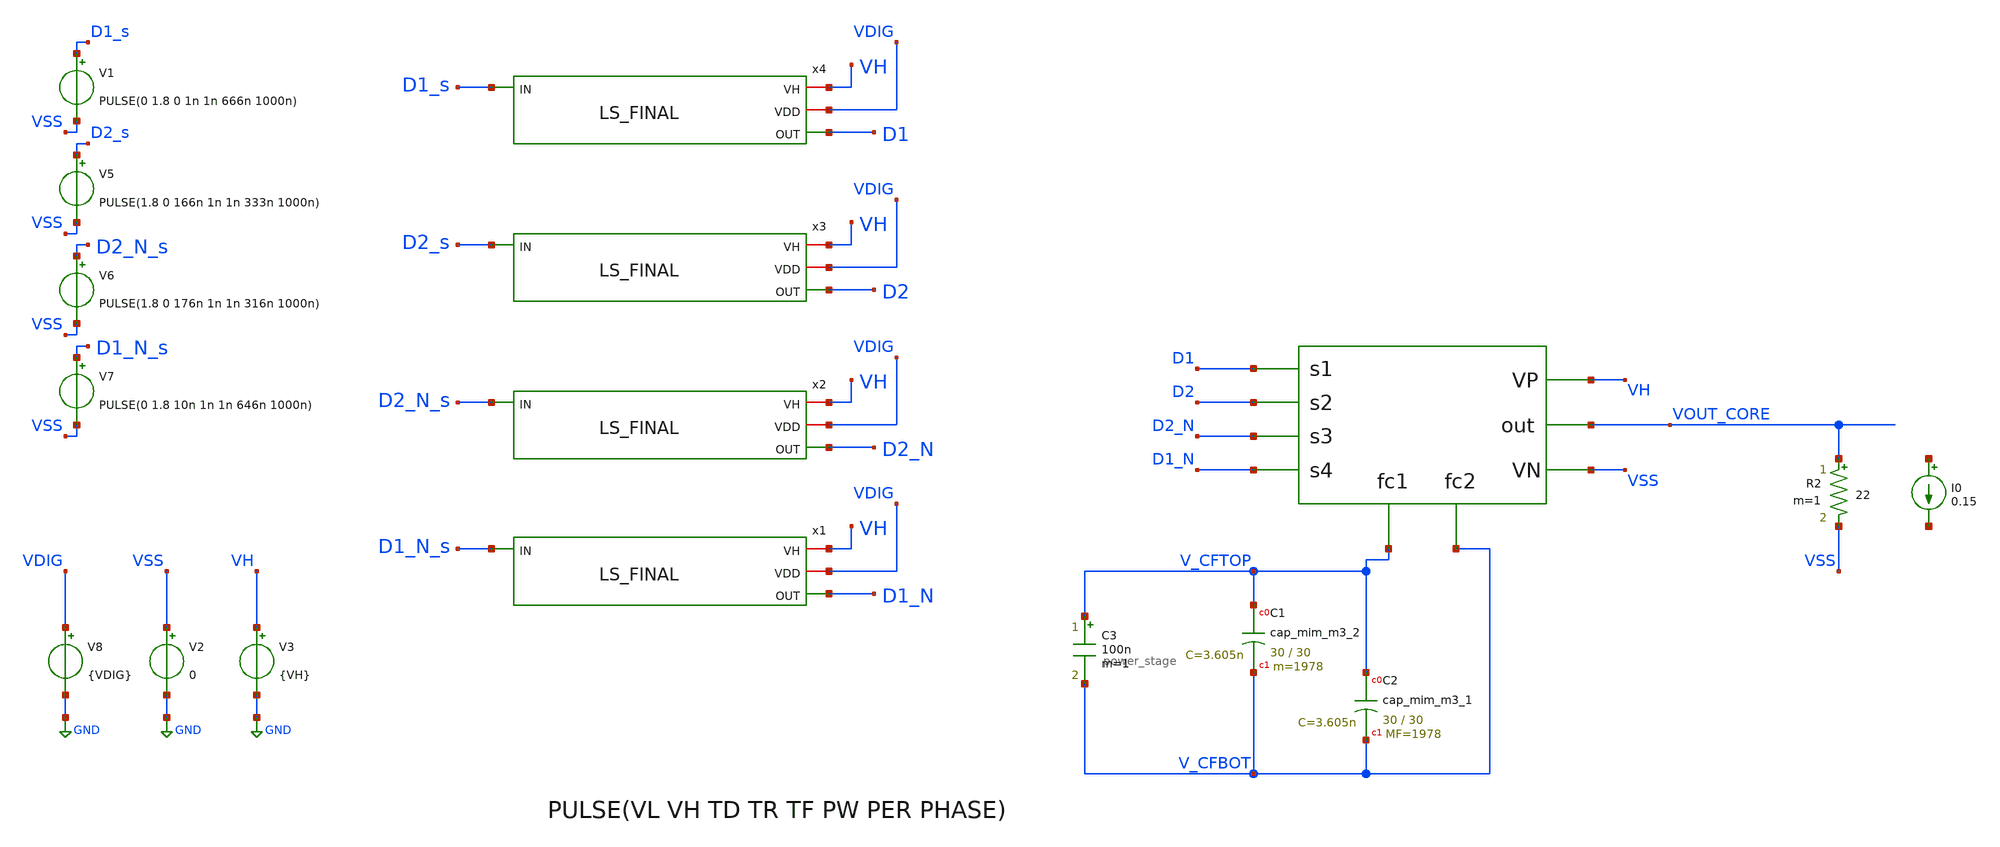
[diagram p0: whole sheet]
** sch_path: xschem/testbench/Interleaved/interleaved_testbench_tomas.sch
**.subckt interleaved_testbench_tomas
V2 VSS GND 0
V3 VH GND {VH}
I0 net1 net2 0.15
R2 VOUT_CORE VSS 22 m=1
XC1 V_CFTOP V_CFBOT sky130_fd_pr__cap_mim_m3_2 W=30 L=30 MF=1978 m=1978
XC2 V_CFTOP V_CFBOT sky130_fd_pr__cap_mim_m3_1 W=30 L=30 MF=1978 m=1978
X2v D1 D2 D2_N D1_N V_CFTOP V_CFBOT VOUT_CORE VH VSS power_stage
V8 VDIG GND {VDIG}
x1 VH VDIG D1_N D1_N_s LS_FINAL
x2 VH VDIG D2_N D2_N_s LS_FINAL
x3 VH VDIG D2 D2_s LS_FINAL
x4 VH VDIG D1 D1_s LS_FINAL
V6 D2_N_s VSS PULSE(1.8 0 176n 1n 1n 316n 1000n)
V5 D2_s VSS PULSE(1.8 0 166n 1n 1n 333n 1000n)
V7 D1_N_s VSS PULSE(0 1.8 10n 1n 1n 646n 1000n)
V1 D1_s VSS PULSE(0 1.8 0 1n 1n 666n 1000n)
C3 V_CFTOP V_CFBOT 100n m=1
**** begin user architecture code


.param VIN = 5
.param VDIG = 1.8
.param VH = 5
.param RL = 50
.option scale=1e-6
*.option temp=70
.ic v(V_CFTOP) = VH/2
.ic v(vout_core)=0
.ic v(V_CFBOT) = 0
*.probe vd(MP2:G:S)
*.save all
*.save v(d1) v(d2) v(d1top_5v) v(d2_5v) v(d2bot_5v) v(d1bot_5v) v(vout) v(vout_core) v(vdd) v(vh) i(v1) i(v5) i(vmeas) v(v_cftop,v_cfbot)
.save v(D1) v(D2) v(D1_N) v(D2_N) v(VOUT_CORE) v(vh) i(v3) v(v_cftop,v_cfbot) v(D1,v_cftop) v(D2,vout_core) v(D2_N,v_cfbot) v(D1_Nv,VSS) v(v_out_ls1) v(v_out_ls2) v(d2_n,v_cfbot)
.save @m.xm4.msky130_fd_pr__nfet_g5v0d10v5[vds]
.param mc_mm_switch=0
*.lib /home/jorge/Documents/Postdoc/share/pdk/sky130A/libs.tech/ngspice/sky130.lib.spice tt
*.lib /usr/share/pdk/sky130A/libs.tech/ngspice/sky130.lib.spice ss
.lib /foss/pdk/sky130A/libs.tech/ngspice/sky130.lib.spice TT
*.include /usr/share/pdk/sky130A/libs.ref/sky130_fd_sc_hvl/spice/sky130_fd_sc_hvl.spice
*.include /home/jorge/Documents/Postdoc/share/pdk/sky130A/libs.ref/sky130_fd_sc_hvl/spice/sky130_fd_sc_hvl.spice
.options savecurrents
.control
*save all
tran 100n 3u
*write DCDC_v1p4_5MHz_NMOS_PMOS.raw
*wrdata
*+ ~/Documents/Postdoc/chipathon2022/3LFCC_AC3E/xschem/dev_switches/DCDC_5V_FINAL/3LFCC_v1p4.txt tran.v(vout) tran.i(vmeas) tran.v(vdd) tran.i(v3) tran.v(vh) tran.i(v5)
*wrdata /foss/designs/personal/3LFCC_AC3E/xschem/hierarchy_sch/DCDC_5V_FINAL/3LFCC_v1p4.txt
*+ tran.v(vout_core) tran.i(v1)
wrdata /foss/designs/personal/3LFCC_AC3E/xschem/testbench/interleaved/3LFCC_v1p5_jm.txt
+ tran.v(vout_core) tran.i(v3)

*Relación D1 D2 para combinar estados
*plot v(D1) v(D2)	v(v_cftop,v_cfbot)
*plot v(D1_N) v(D2_N)

plot v(D1)-v(VH)
plot v(D2)-v(V_CFTOP)
plot v(D2_N)-v(V_CFBOT)
plot v(D1_N)-v(VSS)


*Relación Pulso P y N para acondicionar tiempos muertos (reducir peaks)
*plot v(D1) v(D1_N) v(v_cftop,v_cfbot)
*plot v(D2) v(D2_N) i(v3)
*plot v(D1) v(D1_N)	 v(D2) v(D2_N) i(v3) v(v_cftop,v_cfbot)


*Revisión de estados del convertidor en base a señal de Flycap (caso Cap_ext omitido para ver bien
*+ formas de onda de flycap)
*plot v(v_cftop,v_cfbot) v(vout_core) i(v3)

*plot v(v_cftop,v_cfbot) v(D1) v(D2)
*plot v(v_cftop,v_cfbot) v(D2) v(D2_N)
*plot v(v_cftop,v_cfbot) v(D1) v(D1_N)
*plot v(v_cftop,v_cfbot) v(vout_core)

**Problema actual, eficiencia no se logra calcular debido a que no transicionan bien todo los
*+ estados, (Cuando el Flycap esta flotante no esta consumiendo energía, es decir la carga no esta conectada a
*+ la fuente de entrada...)
** Si bien D1- D1_N y D2- D2_N estan con sus respectivos tiempos muertos (redución de peaks), falta
*+ sincronizar bien D1 con D2 para lograr la conexión correcta para que la carga se conecte a la fuente en estado
*+ de flycap flotante.

.endc


**** end user architecture code
**.ends

* expanding   symbol:  personal/3LFCC_AC3E/xschem/hierarchy_sch/power_stage.sym # of pins=9
** sym_path: xschem/hierarchy_sch/power_stage.sym
** sch_path: xschem/hierarchy_sch/power_stage.sch
.subckt power_stage s1 s2 s3 s4 fc1 fc2 out VP VN
*.ipin s1
*.ipin s2
*.ipin s3
*.ipin s4
*.iopin VP
*.iopin VN
*.opin out
*.opin fc1
*.opin fc2
X1 s2 fc1 s1 VP out transistor_group_one
X2 s4 fc2 s3 out VN transistor_group_two
.ends


* expanding   symbol:  personal/3LFCC_AC3E/xschem/hierarchy_sch/LS_FINAL.sym # of pins=4
** sym_path: xschem/hierarchy_sch/LS_FINAL.sym
** sch_path: xschem/hierarchy_sch/LS_FINAL.sch
.subckt LS_FINAL VH VDD OUT IN
*.ipin IN
*.iopin VDD
*.iopin VH
*.opin OUT
XM11 net1 IN VDD VDD sky130_fd_pr__pfet_01v8 L=0.15 W=1 nf=1 ad='int((nf+1)/2) * W/nf * 0.29' as='int((nf+2)/2) * W/nf * 0.29'
+ pd='2*int((nf+1)/2) * (W/nf + 0.29)' ps='2*int((nf+2)/2) * (W/nf + 0.29)' nrd='0.29 / W' nrs='0.29 / W'
+ sa=0 sb=0 sd=0 mult=5 m=5
XM12 net1 IN GND GND sky130_fd_pr__nfet_01v8 L=0.15 W=1 nf=1 ad='int((nf+1)/2) * W/nf * 0.29' as='int((nf+2)/2) * W/nf * 0.29'
+ pd='2*int((nf+1)/2) * (W/nf + 0.29)' ps='2*int((nf+2)/2) * (W/nf + 0.29)' nrd='0.29 / W' nrs='0.29 / W'
+ sa=0 sb=0 sd=0 mult=5 m=5
XM15 net2 net3 VH VH sky130_fd_pr__pfet_g5v0d10v5 L=0.5 W=2 nf=1 ad='int((nf+1)/2) * W/nf * 0.29' as='int((nf+2)/2) * W/nf * 0.29'
+ pd='2*int((nf+1)/2) * (W/nf + 0.29)' ps='2*int((nf+2)/2) * (W/nf + 0.29)' nrd='0.29 / W' nrs='0.29 / W'
+ sa=0 sb=0 sd=0 mult=1 m=1
XM14 net3 net2 VH VH sky130_fd_pr__pfet_g5v0d10v5 L=0.5 W=2 nf=1 ad='int((nf+1)/2) * W/nf * 0.29' as='int((nf+2)/2) * W/nf * 0.29'
+ pd='2*int((nf+1)/2) * (W/nf + 0.29)' ps='2*int((nf+2)/2) * (W/nf + 0.29)' nrd='0.29 / W' nrs='0.29 / W'
+ sa=0 sb=0 sd=0 mult=1 m=1
XM16 net4 net2 VH VH sky130_fd_pr__pfet_g5v0d10v5 L=0.5 W=10 nf=1 ad='int((nf+1)/2) * W/nf * 0.29' as='int((nf+2)/2) * W/nf * 0.29'
+ pd='2*int((nf+1)/2) * (W/nf + 0.29)' ps='2*int((nf+2)/2) * (W/nf + 0.29)' nrd='0.29 / W' nrs='0.29 / W'
+ sa=0 sb=0 sd=0 mult=10 m=10
XM18 net2 net1 GND GND sky130_fd_pr__nfet_g5v0d10v5 L=0.5 W=4 nf=1 ad='int((nf+1)/2) * W/nf * 0.29' as='int((nf+2)/2) * W/nf * 0.29'
+ pd='2*int((nf+1)/2) * (W/nf + 0.29)' ps='2*int((nf+2)/2) * (W/nf + 0.29)' nrd='0.29 / W' nrs='0.29 / W'
+ sa=0 sb=0 sd=0 mult=3 m=3
XM13 net3 IN GND GND sky130_fd_pr__nfet_g5v0d10v5 L=0.5 W=4 nf=1 ad='int((nf+1)/2) * W/nf * 0.29' as='int((nf+2)/2) * W/nf * 0.29'
+ pd='2*int((nf+1)/2) * (W/nf + 0.29)' ps='2*int((nf+2)/2) * (W/nf + 0.29)' nrd='0.29 / W' nrs='0.29 / W'
+ sa=0 sb=0 sd=0 mult=3 m=3
XM17 net4 IN GND GND sky130_fd_pr__nfet_g5v0d10v5 L=0.5 W=10 nf=1 ad='int((nf+1)/2) * W/nf * 0.29' as='int((nf+2)/2) * W/nf * 0.29'
+ pd='2*int((nf+1)/2) * (W/nf + 0.29)' ps='2*int((nf+2)/2) * (W/nf + 0.29)' nrd='0.29 / W' nrs='0.29 / W'
+ sa=0 sb=0 sd=0 mult=10 m=10
XM7 OUT net4 VH VH sky130_fd_pr__pfet_g5v0d10v5 L=0.5 W=20 nf=1 ad='int((nf+1)/2) * W/nf * 0.29' as='int((nf+2)/2) * W/nf * 0.29'
+ pd='2*int((nf+1)/2) * (W/nf + 0.29)' ps='2*int((nf+2)/2) * (W/nf + 0.29)' nrd='0.29 / W' nrs='0.29 / W'
+ sa=0 sb=0 sd=0 mult=20 m=20
XM10 OUT net4 GND GND sky130_fd_pr__nfet_g5v0d10v5 L=0.5 W=20 nf=1 ad='int((nf+1)/2) * W/nf * 0.29' as='int((nf+2)/2) * W/nf * 0.29'
+ pd='2*int((nf+1)/2) * (W/nf + 0.29)' ps='2*int((nf+2)/2) * (W/nf + 0.29)' nrd='0.29 / W' nrs='0.29 / W'
+ sa=0 sb=0 sd=0 mult=20 m=20
.ends


* expanding   symbol:  personal/3LFCC_AC3E/xschem/hierarchy_sch/transistor_group_one.sym # of pins=5
** sym_path: xschem/hierarchy_sch/transistor_group_one.sym
** sch_path: xschem/hierarchy_sch/transistor_group_one.sch
.subckt transistor_group_one s2 fc1 s1 VP out
*.iopin VP
*.ipin s1
*.ipin s2
*.opin fc1
*.iopin out
XM3 out s2 fc1 fc1 sky130_fd_pr__pfet_g5v0d10v5 L=0.5 W=4.38 nf=1 ad='int((nf+1)/2) * W/nf * 0.29' as='int((nf+2)/2) * W/nf * 0.29'
+ pd='2*int((nf+1)/2) * (W/nf + 0.29)' ps='2*int((nf+2)/2) * (W/nf + 0.29)' nrd='0.29 / W' nrs='0.29 / W'
+ sa=0 sb=0 sd=0 mult=4506 m=4506
XM4 fc1 s1 VP VP sky130_fd_pr__pfet_g5v0d10v5 L=0.5 W=4.38 nf=1 ad='int((nf+1)/2) * W/nf * 0.29' as='int((nf+2)/2) * W/nf * 0.29'
+ pd='2*int((nf+1)/2) * (W/nf + 0.29)' ps='2*int((nf+2)/2) * (W/nf + 0.29)' nrd='0.29 / W' nrs='0.29 / W'
+ sa=0 sb=0 sd=0 mult=4506 m=4506
.ends


* expanding   symbol:  personal/3LFCC_AC3E/xschem/hierarchy_sch/transistor_group_two.sym # of pins=5
** sym_path: xschem/hierarchy_sch/transistor_group_two.sym
** sch_path: xschem/hierarchy_sch/transistor_group_two.sch
.subckt transistor_group_two s4 fc2 s3 out VN
*.iopin out
*.ipin s3
*.ipin s4
*.opin fc2
*.iopin VN
XM1 out s3 fc2 fc2 sky130_fd_pr__nfet_g5v0d10v5 L=0.5 W=4.38 nf=1 ad='int((nf+1)/2) * W/nf * 0.29' as='int((nf+2)/2) * W/nf * 0.29'
+ pd='2*int((nf+1)/2) * (W/nf + 0.29)' ps='2*int((nf+2)/2) * (W/nf + 0.29)' nrd='0.29 / W' nrs='0.29 / W'
+ sa=0 sb=0 sd=0 mult=2520 m=2520
XM2 fc2 s4 VN VN sky130_fd_pr__nfet_g5v0d10v5 L=0.5 W=4.38 nf=1 ad='int((nf+1)/2) * W/nf * 0.29' as='int((nf+2)/2) * W/nf * 0.29'
+ pd='2*int((nf+1)/2) * (W/nf + 0.29)' ps='2*int((nf+2)/2) * (W/nf + 0.29)' nrd='0.29 / W' nrs='0.29 / W'
+ sa=0 sb=0 sd=0 mult=2520 m=2520
.ends

.GLOBAL GND
.end
